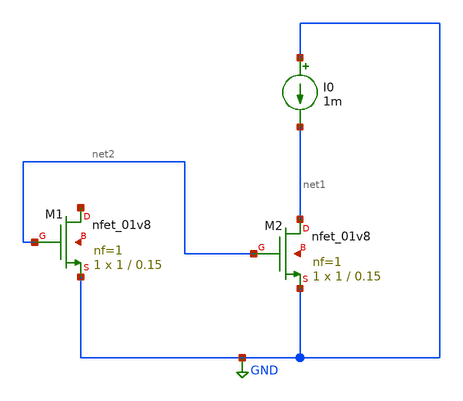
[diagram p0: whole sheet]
** sch_path: currentmirror.sch
**.subckt currentmirror
XM1 net3 net2 GND net4 sky130_fd_pr__nfet_01v8 L=0.15 W=1 nf=1 ad='int((nf+1)/2) * W/nf * 0.29' as='int((nf+2)/2) * W/nf * 0.29'
+ pd='2*int((nf+1)/2) * (W/nf + 0.29)' ps='2*int((nf+2)/2) * (W/nf + 0.29)' nrd='0.29 / W' nrs='0.29 / W'
+ sa=0 sb=0 sd=0 mult=1 m=1
XM2 net1 net2 GND net5 sky130_fd_pr__nfet_01v8 L=0.15 W=1 nf=1 ad='int((nf+1)/2) * W/nf * 0.29' as='int((nf+2)/2) * W/nf * 0.29'
+ pd='2*int((nf+1)/2) * (W/nf + 0.29)' ps='2*int((nf+2)/2) * (W/nf + 0.29)' nrd='0.29 / W' nrs='0.29 / W'
+ sa=0 sb=0 sd=0 mult=1 m=1
I0 GND net1 1m
**.ends
.GLOBAL GND
.end
